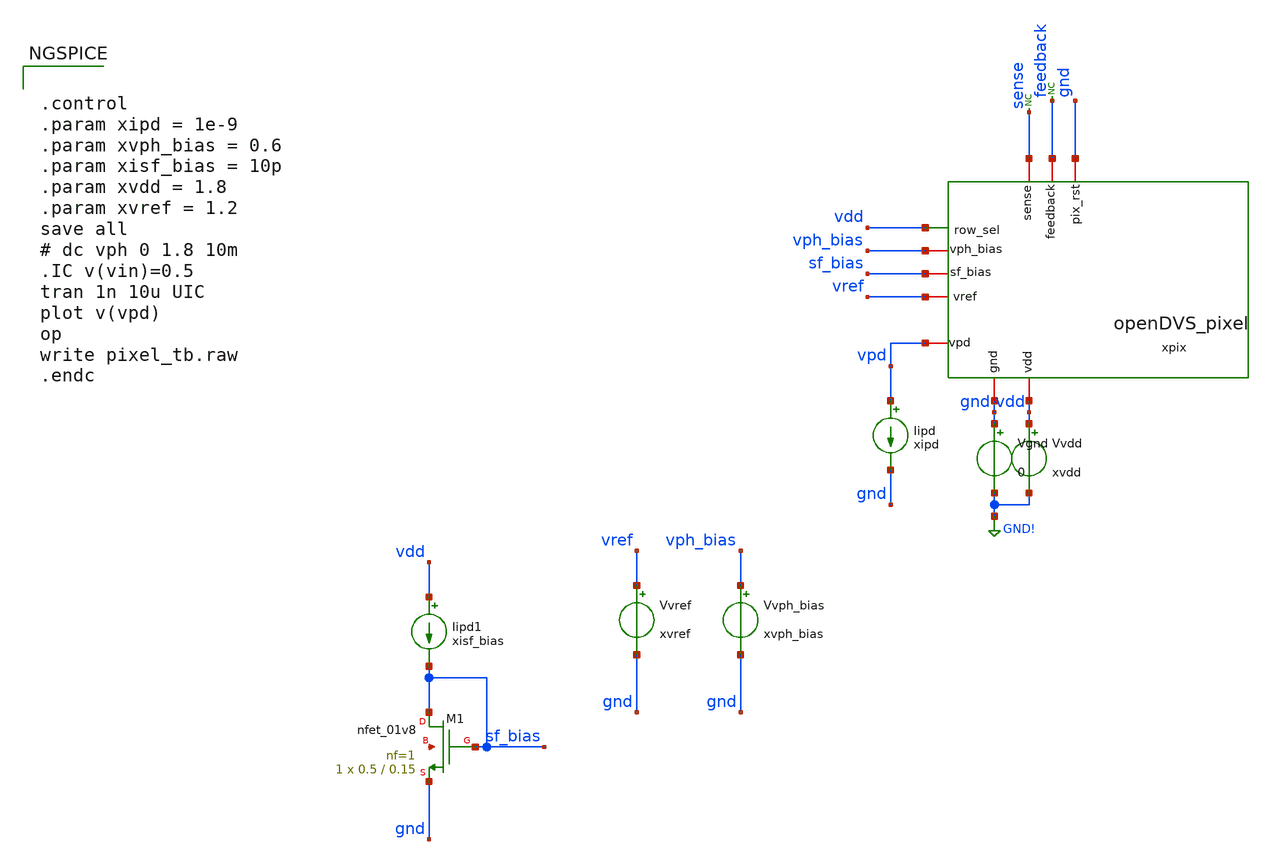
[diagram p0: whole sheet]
** sch_path: analog/xschem/pixel_tb.sch
**.subckt pixel_tb
xpix feedback gnd sense vdd vdd sf_bias gnd vref vpd vph_bias openDVS_pixel
Vgnd gnd GND! 0
Vvdd vdd GND! xvdd
Iipd vpd gnd xipd
XM1 sf_bias sf_bias gnd net1 sky130_fd_pr__nfet_01v8 L=0.15 W=0.5 nf=1 ad='int((1 + 1)/2) * 0.5 / 1 * 0.29'
+ as='int((1 + 2)/2) * 0.5 / 1 * 0.29' pd='2*int((1 + 1)/2) * (0.5 / 1 + 0.29)' ps='2*int((1 + 2)/2) * (0.5 / 1 + 0.29)'
+ nrd='0.29 / 0.5 ' nrs='0.29 / 0.5 ' sa=0 sb=0 sd=0 mult=1 m=1
Iipd1 vdd sf_bias xisf_bias
Vvref vref gnd xvref
Vvph_bias vph_bias gnd xvph_bias
* noconn sense
* noconn feedback
**** begin user architecture code

** opencircuitdesign pdks install
.lib $::SKYWATER_MODELS/sky130.lib.spice tt



.control
.param xipd = 1e-9
.param xvph_bias = 0.6
.param xisf_bias = 10p
.param xvdd = 1.8
.param xvref = 1.2
save all
# dc vph 0 1.8 10m
.IC v(vin)=0.5
tran 1n 10u UIC
plot v(vpd)
op
write pixel_tb.raw
.endc


**** end user architecture code
**.ends

* expanding   symbol:  openDVS_pixel.sym # of pins=10
** sym_path: analog/xschem/openDVS_pixel.sym
** sch_path: analog/xschem/openDVS_pixel.sch
.subckt openDVS_pixel feedback pix_rst sense row_sel vdd sf_bias gnd vref vpd vph_bias
*.ipin row_sel
*.iopin sense
*.iopin pix_rst
*.iopin feedback
*.iopin vph_bias
*.iopin vdd
*.iopin vref
*.iopin vpd
*.iopin sf_bias
*.iopin gnd
XCSAMPLE vph_sf vd sky130_fd_pr__cap_mim_m3_1 W=1 L=1 MF=16 m=16
XCREF vref vd sky130_fd_pr__cap_mim_m3_1 W=1 L=1 MF=2 m=2
XMpd vdd vph_bias vpd gnd sky130_fd_pr__nfet_01v8 L=0.15 W=0.5 nf=1 ad='int((1 + 1)/2) * 0.5 / 1 * 0.29'
+ as='int((1 + 2)/2) * 0.5 / 1 * 0.29' pd='2*int((1 + 1)/2) * (0.5 / 1 + 0.29)' ps='2*int((1 + 2)/2) * (0.5 / 1 + 0.29)'
+ nrd='0.29 / 0.5 ' nrs='0.29 / 0.5 ' sa=0 sb=0 sd=0 mult=1 m=1
XMch_amp sense_local vd gnd gnd sky130_fd_pr__nfet_01v8 L=0.15 W=2 nf=1 ad='int((1 + 1)/2) * 2 / 1 * 0.29'
+ as='int((1 + 2)/2) * 2 / 1 * 0.29' pd='2*int((1 + 1)/2) * (2 / 1 + 0.29)' ps='2*int((1 + 2)/2) * (2 / 1 + 0.29)'
+ nrd='0.29 / 2 ' nrs='0.29 / 2 ' sa=0 sb=0 sd=0 mult=1 m=1
XMsw feedback lrst vd gnd sky130_fd_pr__nfet_01v8 L=0.15 W=1 nf=1 ad='int((1 + 1)/2) * 1 / 1 * 0.29'
+ as='int((1 + 2)/2) * 1 / 1 * 0.29' pd='2*int((1 + 1)/2) * (1 / 1 + 0.29)' ps='2*int((1 + 2)/2) * (1 / 1 + 0.29)'
+ nrd='0.29 / 1 ' nrs='0.29 / 1 ' sa=0 sb=0 sd=0 mult=1 m=1
XMsf_bias vph_sf sf_bias gnd gnd sky130_fd_pr__nfet_01v8 L=0.15 W=0.5 nf=1 ad='int((1 + 1)/2) * 0.5 / 1 * 0.29'
+ as='int((1 + 2)/2) * 0.5 / 1 * 0.29' pd='2*int((1 + 1)/2) * (0.5 / 1 + 0.29)' ps='2*int((1 + 2)/2) * (0.5 / 1 + 0.29)'
+ nrd='0.29 / 0.5 ' nrs='0.29 / 0.5 ' sa=0 sb=0 sd=0 mult=1 m=1
XMsf vdd vpd vph_sf gnd sky130_fd_pr__nfet_01v8 L=0.15 W=0.5 nf=1 ad='int((1 + 1)/2) * 0.5 / 1 * 0.29'
+ as='int((1 + 2)/2) * 0.5 / 1 * 0.29' pd='2*int((1 + 1)/2) * (0.5 / 1 + 0.29)' ps='2*int((1 + 2)/2) * (0.5 / 1 + 0.29)'
+ nrd='0.29 / 0.5 ' nrs='0.29 / 0.5 ' sa=0 sb=0 sd=0 mult=1 m=1
XMrow_sel sense row_sel sense_local gnd sky130_fd_pr__nfet_01v8 L=0.15 W=1 nf=1 ad='int((1 + 1)/2) * 1 / 1 * 0.29'
+ as='int((1 + 2)/2) * 1 / 1 * 0.29' pd='2*int((1 + 1)/2) * (1 / 1 + 0.29)' ps='2*int((1 + 2)/2) * (1 / 1 + 0.29)'
+ nrd='0.29 / 1 ' nrs='0.29 / 1 ' sa=0 sb=0 sd=0 mult=1 m=1
XMfb_row_sel pix_rst row_sel lrst gnd sky130_fd_pr__nfet_01v8 L=0.15 W=1 nf=1 ad='int((1 + 1)/2) * 1 / 1 * 0.29'
+ as='int((1 + 2)/2) * 1 / 1 * 0.29' pd='2*int((1 + 1)/2) * (1 / 1 + 0.29)' ps='2*int((1 + 2)/2) * (1 / 1 + 0.29)'
+ nrd='0.29 / 1 ' nrs='0.29 / 1 ' sa=0 sb=0 sd=0 mult=1 m=1
XDpd gnd vpd sky130_fd_pr__photodiode area=9e-12 perim=12e-6
.ends

.GLOBAL GND!
.end
